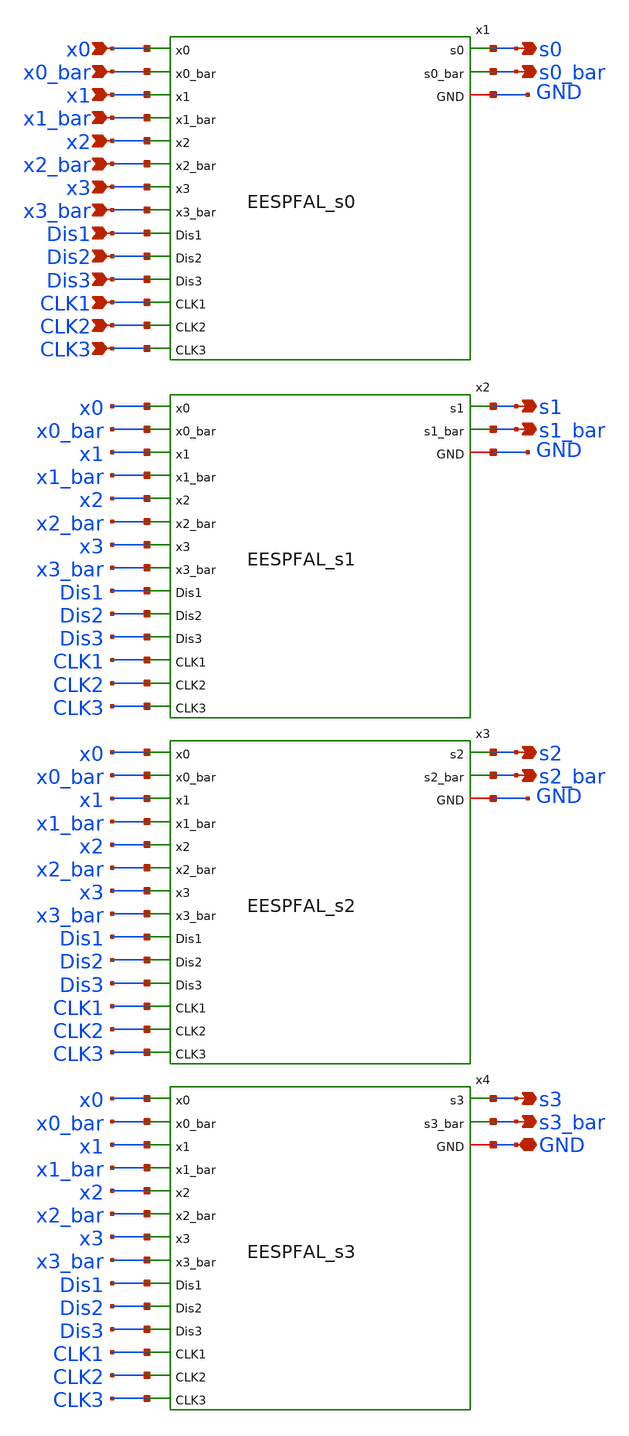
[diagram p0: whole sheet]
** sch_path: skywater_stuff/untitled-12.sch
**.subckt untitled-12 GND s3_bar s3 x0 s2_bar s2 s1_bar s1 s0_bar s0 x0_bar x1 x1_bar x2 x2_bar x3
*+ x3_bar Dis1 Dis2 Dis3 CLK1 CLK2 CLK3
*.iopin GND
*.opin s3_bar
*.opin s3
*.ipin x0
*.opin s2_bar
*.opin s2
*.opin s1_bar
*.opin s1
*.opin s0_bar
*.opin s0
*.ipin x0_bar
*.ipin x1
*.ipin x1_bar
*.ipin x2
*.ipin x2_bar
*.ipin x3
*.ipin x3_bar
*.ipin Dis1
*.ipin Dis2
*.ipin Dis3
*.ipin CLK1
*.ipin CLK2
*.ipin CLK3
x1 GND x0 x0_bar x1 x1_bar x2 x2_bar x3 x3_bar CLK1 Dis1 CLK3 Dis2 CLK2 Dis3 s0 s0_bar EESPFAL_s0
x2 GND x0 x0_bar x1 x1_bar x2 x2_bar x3 x3_bar s1_bar s1 CLK1 Dis1 Dis3 CLK3 Dis2 CLK2 EESPFAL_s1
x3 GND x0 x0_bar x1 x1_bar x2 x2_bar x3 x3_bar CLK1 Dis1 Dis3 Dis2 CLK3 CLK2 s2_bar s2 EESPFAL_s2
x4 GND x0 x0_bar x1 x1_bar x2 x2_bar x3 x3_bar s3_bar CLK1 s3 Dis1 Dis3 CLK3 Dis2 CLK2 EESPFAL_s3
**.ends
.end
